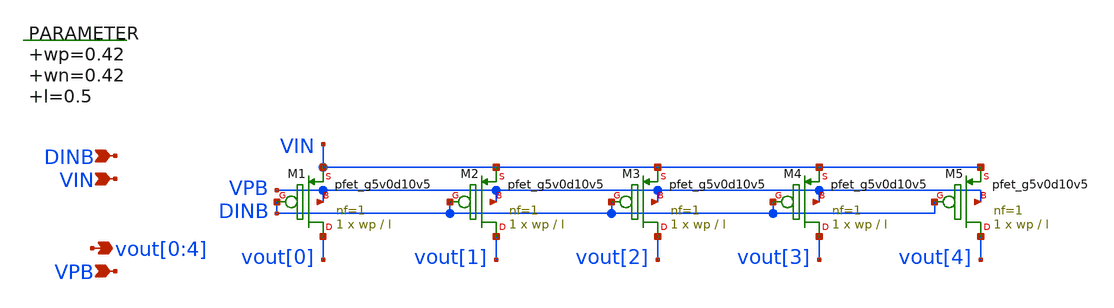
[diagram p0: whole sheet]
** sch_path: xschem/seg_selector_4.sch
**.subckt seg_selector_4 vout[0],vout[1],vout[2],vout[3],vout[4] VPB DINB VIN
*.opin vout[0],vout[1],vout[2],vout[3],vout[4]
*.ipin VPB
*.ipin DINB
*.ipin VIN
.param wp=0.42 wn=0.42 l=0.5

XM1 vout[0] DINB VIN VPB sky130_fd_pr__pfet_g5v0d10v5 L=l W=wp nf=1 ad='int((nf+1)/2) * W/nf * 0.29'
+ as='int((nf+2)/2) * W/nf * 0.29' pd='2*int((nf+1)/2) * (W/nf + 0.29)' ps='2*int((nf+2)/2) * (W/nf + 0.29)'
+ nrd='0.29 / W' nrs='0.29 / W' sa=0 sb=0 sd=0 mult=1 m=1
XM2 vout[1] DINB VIN VPB sky130_fd_pr__pfet_g5v0d10v5 L=l W=wp nf=1 ad='int((nf+1)/2) * W/nf * 0.29'
+ as='int((nf+2)/2) * W/nf * 0.29' pd='2*int((nf+1)/2) * (W/nf + 0.29)' ps='2*int((nf+2)/2) * (W/nf + 0.29)'
+ nrd='0.29 / W' nrs='0.29 / W' sa=0 sb=0 sd=0 mult=1 m=1
XM3 vout[2] DINB VIN VPB sky130_fd_pr__pfet_g5v0d10v5 L=l W=wp nf=1 ad='int((nf+1)/2) * W/nf * 0.29'
+ as='int((nf+2)/2) * W/nf * 0.29' pd='2*int((nf+1)/2) * (W/nf + 0.29)' ps='2*int((nf+2)/2) * (W/nf + 0.29)'
+ nrd='0.29 / W' nrs='0.29 / W' sa=0 sb=0 sd=0 mult=1 m=1
XM4 vout[3] DINB VIN VPB sky130_fd_pr__pfet_g5v0d10v5 L=l W=wp nf=1 ad='int((nf+1)/2) * W/nf * 0.29'
+ as='int((nf+2)/2) * W/nf * 0.29' pd='2*int((nf+1)/2) * (W/nf + 0.29)' ps='2*int((nf+2)/2) * (W/nf + 0.29)'
+ nrd='0.29 / W' nrs='0.29 / W' sa=0 sb=0 sd=0 mult=1 m=1
XM5 vout[4] DINB VIN VPB sky130_fd_pr__pfet_g5v0d10v5 L=l W=wp nf=1 ad='int((nf+1)/2) * W/nf * 0.29'
+ as='int((nf+2)/2) * W/nf * 0.29' pd='2*int((nf+1)/2) * (W/nf + 0.29)' ps='2*int((nf+2)/2) * (W/nf + 0.29)'
+ nrd='0.29 / W' nrs='0.29 / W' sa=0 sb=0 sd=0 mult=1 m=1
**.ends
.end
